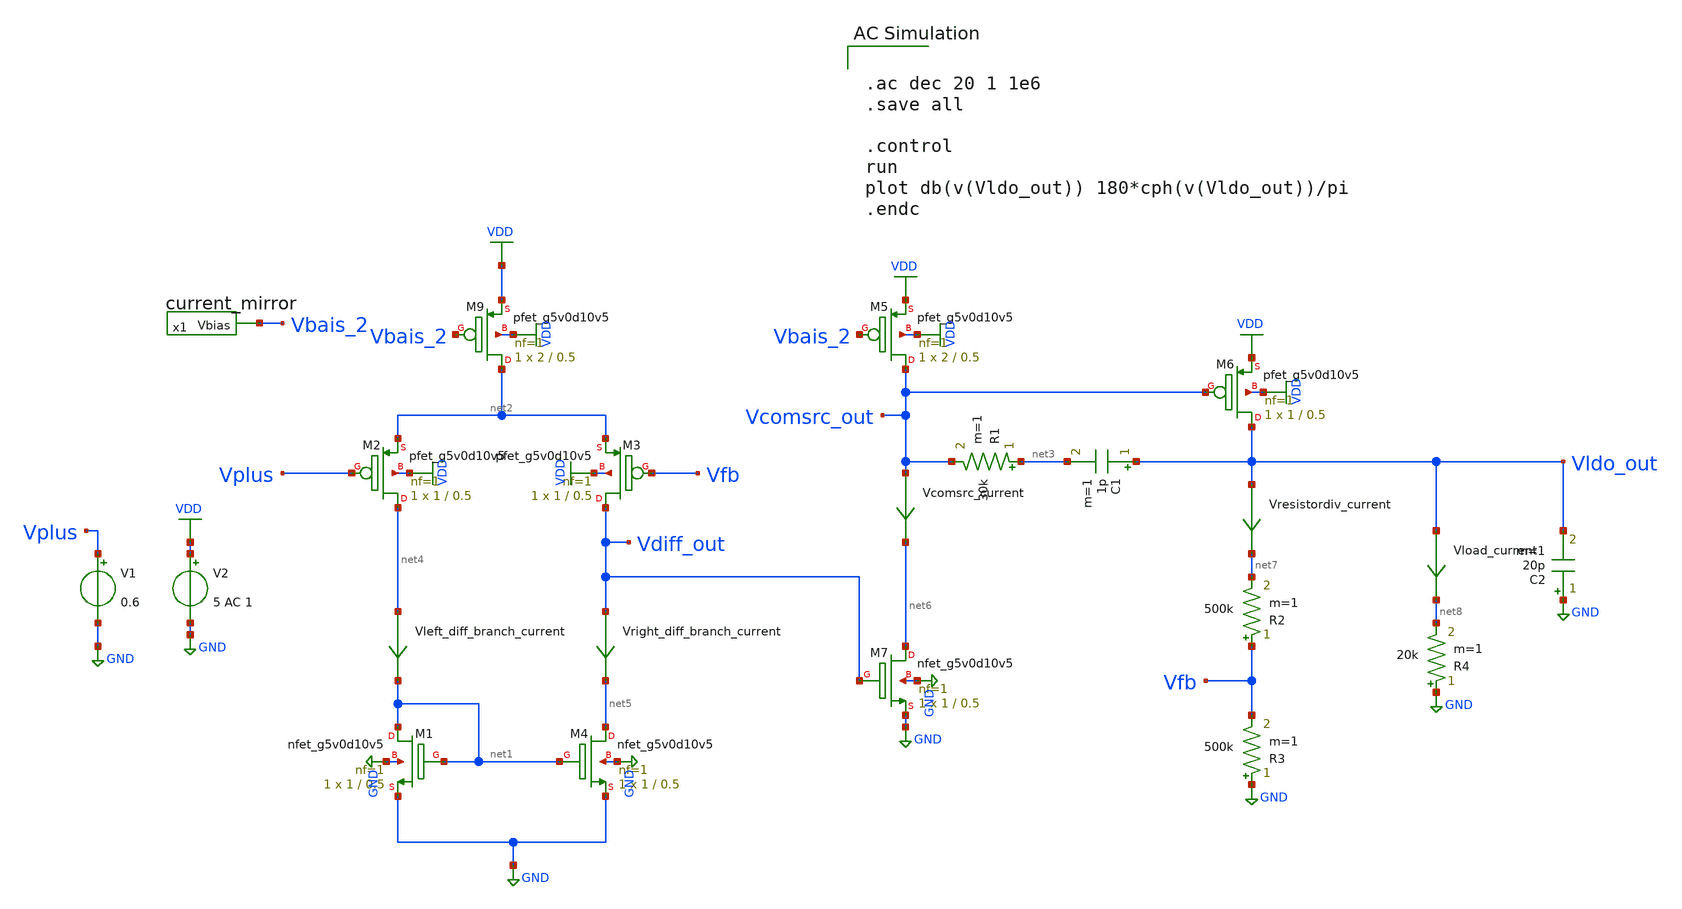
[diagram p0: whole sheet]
** sch_path: Abishek_Sam_group/template/LDO.sch
**.subckt LDO
XM1 net1 net1 GND GND sky130_fd_pr__nfet_g5v0d10v5 L=0.5 W=1 nf=1 ad='int((nf+1)/2) * W/nf * 0.29' as='int((nf+2)/2) * W/nf * 0.29'
+ pd='2*int((nf+1)/2) * (W/nf + 0.29)' ps='2*int((nf+2)/2) * (W/nf + 0.29)' nrd='0.29 / W' nrs='0.29 / W'
+ sa=0 sb=0 sd=0 mult=1 m=1
R1 net3 Vcomsrc_out 30k m=1
C1 Vldo_out net3 1p m=1
x1 Vbais_2 current_mirror
XM4 net5 net1 GND GND sky130_fd_pr__nfet_g5v0d10v5 L=0.5 W=1 nf=1 ad='int((nf+1)/2) * W/nf * 0.29' as='int((nf+2)/2) * W/nf * 0.29'
+ pd='2*int((nf+1)/2) * (W/nf + 0.29)' ps='2*int((nf+2)/2) * (W/nf + 0.29)' nrd='0.29 / W' nrs='0.29 / W'
+ sa=0 sb=0 sd=0 mult=1 m=1
V1 Vplus GND 0.6
XM7 net6 Vdiff_out GND GND sky130_fd_pr__nfet_g5v0d10v5 L=0.5 W=1 nf=1 ad='int((nf+1)/2) * W/nf * 0.29'
+ as='int((nf+2)/2) * W/nf * 0.29' pd='2*int((nf+1)/2) * (W/nf + 0.29)' ps='2*int((nf+2)/2) * (W/nf + 0.29)'
+ nrd='0.29 / W' nrs='0.29 / W' sa=0 sb=0 sd=0 mult=1 m=1
R2 Vfb net7 500k m=1
R3 GND Vfb 500k m=1
R4 GND net8 20k m=1
C2 GND Vldo_out 20p m=1
V2 VDD GND 5 AC 1
Vleft_diff_branch_current net4 net1 0
.save i(vleft_diff_branch_current)
Vright_diff_branch_current Vdiff_out net5 0
.save i(vright_diff_branch_current)
Vcomsrc_current Vcomsrc_out net6 0
.save i(vcomsrc_current)
Vresistordiv_current Vldo_out net7 0
.save i(vresistordiv_current)
Vload_current Vldo_out net8 0
.save i(vload_current)
XM9 net2 Vbais_2 VDD VDD sky130_fd_pr__pfet_g5v0d10v5 L=0.5 W=2 nf=1 ad='int((nf+1)/2) * W/nf * 0.29'
+ as='int((nf+2)/2) * W/nf * 0.29' pd='2*int((nf+1)/2) * (W/nf + 0.29)' ps='2*int((nf+2)/2) * (W/nf + 0.29)'
+ nrd='0.29 / W' nrs='0.29 / W' sa=0 sb=0 sd=0 mult=1 m=1
XM2 net4 Vplus net2 VDD sky130_fd_pr__pfet_g5v0d10v5 L=0.5 W=1 nf=1 ad='int((nf+1)/2) * W/nf * 0.29'
+ as='int((nf+2)/2) * W/nf * 0.29' pd='2*int((nf+1)/2) * (W/nf + 0.29)' ps='2*int((nf+2)/2) * (W/nf + 0.29)'
+ nrd='0.29 / W' nrs='0.29 / W' sa=0 sb=0 sd=0 mult=1 m=1
XM3 Vdiff_out Vfb net2 VDD sky130_fd_pr__pfet_g5v0d10v5 L=0.5 W=1 nf=1 ad='int((nf+1)/2) * W/nf * 0.29'
+ as='int((nf+2)/2) * W/nf * 0.29' pd='2*int((nf+1)/2) * (W/nf + 0.29)' ps='2*int((nf+2)/2) * (W/nf + 0.29)'
+ nrd='0.29 / W' nrs='0.29 / W' sa=0 sb=0 sd=0 mult=1 m=1
XM5 Vcomsrc_out Vbais_2 VDD VDD sky130_fd_pr__pfet_g5v0d10v5 L=0.5 W=2 nf=1 ad='int((nf+1)/2) * W/nf * 0.29'
+ as='int((nf+2)/2) * W/nf * 0.29' pd='2*int((nf+1)/2) * (W/nf + 0.29)' ps='2*int((nf+2)/2) * (W/nf + 0.29)'
+ nrd='0.29 / W' nrs='0.29 / W' sa=0 sb=0 sd=0 mult=1 m=1
XM6 Vldo_out Vcomsrc_out VDD VDD sky130_fd_pr__pfet_g5v0d10v5 L=0.5 W=1 nf=1 ad='int((nf+1)/2) * W/nf * 0.29'
+ as='int((nf+2)/2) * W/nf * 0.29' pd='2*int((nf+1)/2) * (W/nf + 0.29)' ps='2*int((nf+2)/2) * (W/nf + 0.29)'
+ nrd='0.29 / W' nrs='0.29 / W' sa=0 sb=0 sd=0 mult=1 m=1
**** begin user architecture code


.ac dec 20 1 1e6
.save all

.control
run
plot db(v(Vldo_out)) 180*cph(v(Vldo_out))/pi
.endc



.lib $::SKYWATER_MODELS/sky130.lib.spice tt

**** end user architecture code
**.ends

* expanding   symbol:  current_mirror.sym # of pins=1
** sym_path: Abishek_Sam_group/template/current_mirror.sym
** sch_path: Abishek_Sam_group/template/current_mirror.sch
.subckt current_mirror Vbias
*.opin Vbias
XM1 Vbias Vbias VDD VDD sky130_fd_pr__pfet_g5v0d10v5 L=0.5 W=2 nf=1 ad='int((nf+1)/2) * W/nf * 0.29'
+ as='int((nf+2)/2) * W/nf * 0.29' pd='2*int((nf+1)/2) * (W/nf + 0.29)' ps='2*int((nf+2)/2) * (W/nf + 0.29)'
+ nrd='0.29 / W' nrs='0.29 / W' sa=0 sb=0 sd=0 mult=1 m=1
I0 Vbias GND 3u
.ends

.GLOBAL VDD
.GLOBAL GND
.end
